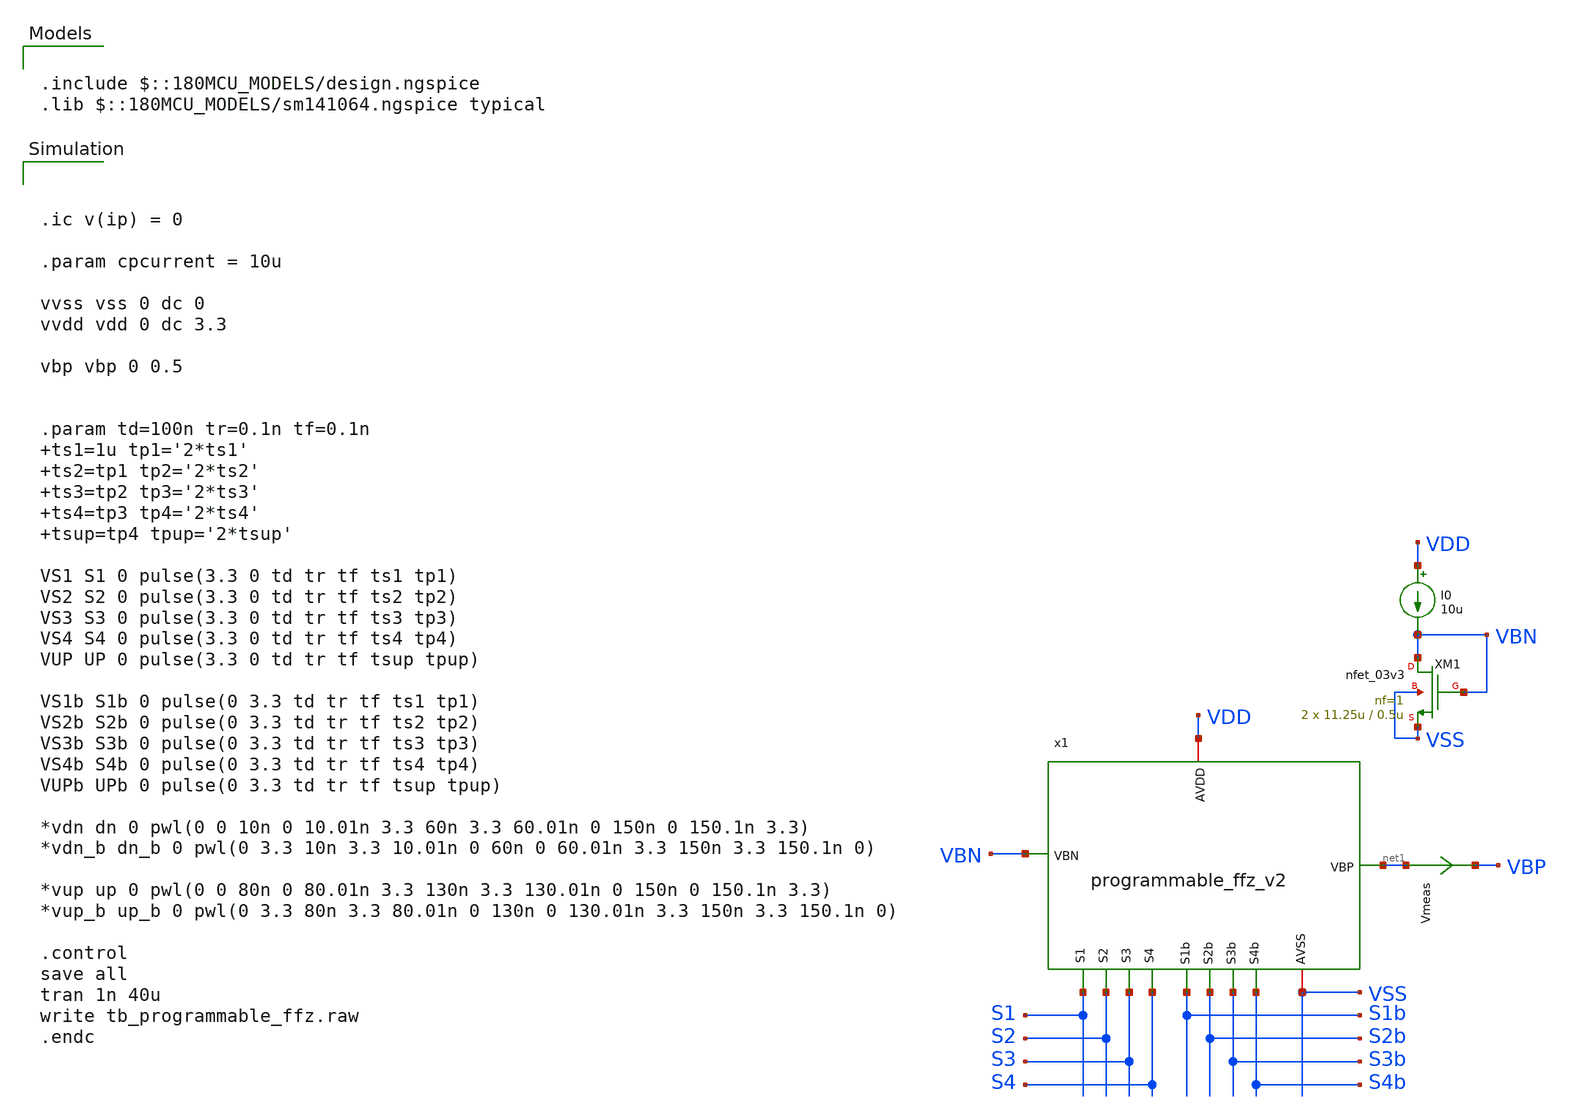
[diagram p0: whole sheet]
** sch_path: designs/libs/tb_analog/tb_programmable_ffz/tb_programmable_ffz_v2.sch
**.subckt tb_programmable_ffz_v2
Vmeas net1 VBP 0
.save i(vmeas)
XM1 VBN VBN VSS VSS nfet_03v3 L=0.5u W=11.25u nf=1 ad='int((nf+1)/2) * W/nf * 0.18u' as='int((nf+2)/2) * W/nf * 0.18u'
+ pd='2*int((nf+1)/2) * (W/nf + 0.18u)' ps='2*int((nf+2)/2) * (W/nf + 0.18u)' nrd='0.18u / W' nrs='0.18u / W'
+ sa=0 sb=0 sd=0 m=2
I0 VDD VBN 10u
x1 VSS VDD net1 VBN S1b S1 S2b S2 S3b S3 S4b S4 programmable_ffz_v2
**** begin user architecture code



.ic v(ip) = 0

.param cpcurrent = 10u

vvss vss 0 dc 0
vvdd vdd 0 dc 3.3

vbp vbp 0 0.5


.param td=100n tr=0.1n tf=0.1n ts1=1u tp1='2*ts1' ts2=tp1 tp2='2*ts2' ts3=tp2 tp3='2*ts3' ts4=tp3 tp4='2*ts4'
+ tsup=tp4 tpup='2*tsup'

VS1 S1 0 pulse(3.3 0 td tr tf ts1 tp1)
VS2 S2 0 pulse(3.3 0 td tr tf ts2 tp2)
VS3 S3 0 pulse(3.3 0 td tr tf ts3 tp3)
VS4 S4 0 pulse(3.3 0 td tr tf ts4 tp4)
VUP UP 0 pulse(3.3 0 td tr tf tsup tpup)

VS1b S1b 0 pulse(0 3.3 td tr tf ts1 tp1)
VS2b S2b 0 pulse(0 3.3 td tr tf ts2 tp2)
VS3b S3b 0 pulse(0 3.3 td tr tf ts3 tp3)
VS4b S4b 0 pulse(0 3.3 td tr tf ts4 tp4)
VUPb UPb 0 pulse(0 3.3 td tr tf tsup tpup)

*vdn dn 0 pwl(0 0 10n 0 10.01n 3.3 60n 3.3 60.01n 0 150n 0 150.1n 3.3)
*vdn_b dn_b 0 pwl(0 3.3 10n 3.3 10.01n 0 60n 0 60.01n 3.3 150n 3.3 150.1n 0)

*vup up 0 pwl(0 0 80n 0 80.01n 3.3 130n 3.3 130.01n 0 150n 0 150.1n 3.3)
*vup_b up_b 0 pwl(0 3.3 80n 3.3 80.01n 0 130n 0 130.01n 3.3 150n 3.3 150.1n 0)

.control
save all
tran 1n 40u
write tb_programmable_ffz.raw
.endc



.include $::180MCU_MODELS/design.ngspice
.lib $::180MCU_MODELS/sm141064.ngspice typical

**** end user architecture code
**.ends

* expanding   symbol:  libs/core_analog/programmable_ffz/programmable_ffz_v2.sym # of pins=12
** sym_path: designs/libs/core_analog/programmable_ffz/programmable_ffz_v2.sym
** sch_path: designs/libs/core_analog/programmable_ffz/programmable_ffz_v2.sch
.subckt programmable_ffz_v2 AVSS AVDD VBP VBN S1b S1 S2b S2 S3b S3 S4b S4
*.ipin VBN
*.ipin S1b
*.ipin S1
*.ipin S2b
*.ipin S2
*.ipin S3b
*.ipin S3
*.ipin S4b
*.ipin S4
*.iopin AVSS
*.iopin AVDD
*.opin VBP
x2 VBN AVSS S1 VBN1 S1b AVDD transmission_gate
x3 VBN AVSS S2 VBN2 S2b AVDD transmission_gate
x4 VBN AVSS S3 VBN3 S3b AVDD transmission_gate
x5 VBN AVSS S4 VBN4 S4b AVDD transmission_gate
x7 VBP_B AVSS S1 VBP S1b AVDD transmission_gate
x81 VBP_C AVSS S2 VBP S2b AVDD transmission_gate
x82 VBP_C AVSS S2 VBP S2b AVDD transmission_gate
x91 VBP_D AVSS S3 VBP S3b AVDD transmission_gate
x92 VBP_D AVSS S3 VBP S3b AVDD transmission_gate
x93 VBP_D AVSS S3 VBP S3b AVDD transmission_gate
x94 VBP_D AVSS S3 VBP S3b AVDD transmission_gate
x101 VBP_E AVSS S4 VBP S4b AVDD transmission_gate
x102 VBP_E AVSS S4 VBP S4b AVDD transmission_gate
x103 VBP_E AVSS S4 VBP S4b AVDD transmission_gate
x104 VBP_E AVSS S4 VBP S4b AVDD transmission_gate
x105 VBP_E AVSS S4 VBP S4b AVDD transmission_gate
x106 VBP_E AVSS S4 VBP S4b AVDD transmission_gate
x107 VBP_E AVSS S4 VBP S4b AVDD transmission_gate
x108 VBP_E AVSS S4 VBP S4b AVDD transmission_gate
x8 VBP_E VBP VBP_C VBN4 VBN VBN2 S4b AVSS S2b AVDD AVSS VBP_B VBP_D VBN1 VBN3 S3b S1b
+ feed_forward_zero_v2_merged
.ends


* expanding   symbol:  libs/core_analog/transmission_gate/transmission_gate.sym # of pins=6
** sym_path: designs/libs/core_analog/transmission_gate/transmission_gate.sym
** sch_path: designs/libs/core_analog/transmission_gate/transmission_gate.sch
.subckt transmission_gate ind vss clkn ins clkp vdd
*.iopin ind
*.iopin ins
*.iopin clkn
*.iopin clkp
*.iopin vdd
*.iopin vss
XM1 ind clkp ins vdd pfet_03v3 L=0.5u W=3.0u nf=1 ad='int((nf+1)/2) * W/nf * 0.18u' as='int((nf+2)/2) * W/nf * 0.18u'
+ pd='2*int((nf+1)/2) * (W/nf + 0.18u)' ps='2*int((nf+2)/2) * (W/nf + 0.18u)' nrd='0.18u / W' nrs='0.18u / W'
+ sa=0 sb=0 sd=0 m=1
XM2 ind clkn ins vss nfet_03v3 L=0.5u W=1.0u nf=1 ad='int((nf+1)/2) * W/nf * 0.18u' as='int((nf+2)/2) * W/nf * 0.18u'
+ pd='2*int((nf+1)/2) * (W/nf + 0.18u)' ps='2*int((nf+2)/2) * (W/nf + 0.18u)' nrd='0.18u / W' nrs='0.18u / W'
+ sa=0 sb=0 sd=0 m=1
.ends


* expanding   symbol:  libs/core_analog/feed_forward_zero/feed_forward_zero_v2_merged.sym # of
*+ pins=17
** sym_path: designs/libs/core_analog/feed_forward_zero/feed_forward_zero_v2_merged.sym
** sch_path: designs/libs/core_analog/feed_forward_zero/feed_forward_zero_v2_merged.sch
.subckt feed_forward_zero_v2_merged VBP_E VBP_A VBP_C VBN_E VBN_A VBN_C S_E S_A S_C AVDD AVSS VBP_B
+ VBP_D VBN_B VBN_D S_D S_B
*.opin VBP_E
*.iopin AVDD
*.ipin VBN_A
*.opin VBP_A
*.ipin VBN_B
*.ipin S_B
*.opin VBP_B
*.ipin VBN_C
*.ipin S_C
*.opin VBP_C
*.ipin VBN_D
*.ipin S_D
*.opin VBP_D
*.ipin VBN_E
*.ipin S_E
*.ipin S_A
*.iopin AVSS
XM1 VBP_A VBP_A AVDD AVDD pfet_03v3 L=1.5u W=1.1u nf=1 ad='int((nf+1)/2) * W/nf * 0.18u' as='int((nf+2)/2) * W/nf * 0.18u'
+ pd='2*int((nf+1)/2) * (W/nf + 0.18u)' ps='2*int((nf+2)/2) * (W/nf + 0.18u)' nrd='0.18u / W' nrs='0.18u / W'
+ sa=0 sb=0 sd=0 m=1
XM3 VBP_A AVDD net1 AVSS nfet_03v3 L=0.5u W=2.08u nf=1 ad='int((nf+1)/2) * W/nf * 0.18u' as='int((nf+2)/2) * W/nf * 0.18u'
+ pd='2*int((nf+1)/2) * (W/nf + 0.18u)' ps='2*int((nf+2)/2) * (W/nf + 0.18u)' nrd='0.18u / W' nrs='0.18u / W'
+ sa=0 sb=0 sd=0 m=1
XM4 net1 VBN_A AVSS AVSS nfet_03v3 L=0.5u W=2.82u nf=1 ad='int((nf+1)/2) * W/nf * 0.18u' as='int((nf+2)/2) * W/nf * 0.18u'
+ pd='2*int((nf+1)/2) * (W/nf + 0.18u)' ps='2*int((nf+2)/2) * (W/nf + 0.18u)' nrd='0.18u / W' nrs='0.18u / W'
+ sa=0 sb=0 sd=0 m=4
XM7 VBN_A S_A AVSS AVSS nfet_03v3 L=0.5u W=1u nf=1 ad='int((nf+1)/2) * W/nf * 0.18u' as='int((nf+2)/2) * W/nf * 0.18u'
+ pd='2*int((nf+1)/2) * (W/nf + 0.18u)' ps='2*int((nf+2)/2) * (W/nf + 0.18u)' nrd='0.18u / W' nrs='0.18u / W'
+ sa=0 sb=0 sd=0 m=1
XM2 VBP_A VBP_A AVDD AVDD pfet_03v3 L=1.5u W=1.1u nf=1 ad='int((nf+1)/2) * W/nf * 0.18u' as='int((nf+2)/2) * W/nf * 0.18u'
+ pd='2*int((nf+1)/2) * (W/nf + 0.18u)' ps='2*int((nf+2)/2) * (W/nf + 0.18u)' nrd='0.18u / W' nrs='0.18u / W'
+ sa=0 sb=0 sd=0 m=1
XM5 VBP_B VBP_B AVDD AVDD pfet_03v3 L=1.5u W=1.1u nf=1 ad='int((nf+1)/2) * W/nf * 0.18u' as='int((nf+2)/2) * W/nf * 0.18u'
+ pd='2*int((nf+1)/2) * (W/nf + 0.18u)' ps='2*int((nf+2)/2) * (W/nf + 0.18u)' nrd='0.18u / W' nrs='0.18u / W'
+ sa=0 sb=0 sd=0 m=1
XM6 VBP_B AVDD net2 AVSS nfet_03v3 L=0.5u W=2.08u nf=1 ad='int((nf+1)/2) * W/nf * 0.18u' as='int((nf+2)/2) * W/nf * 0.18u'
+ pd='2*int((nf+1)/2) * (W/nf + 0.18u)' ps='2*int((nf+2)/2) * (W/nf + 0.18u)' nrd='0.18u / W' nrs='0.18u / W'
+ sa=0 sb=0 sd=0 m=1
XM8 net2 VBN_B AVSS AVSS nfet_03v3 L=0.5u W=2.82u nf=1 ad='int((nf+1)/2) * W/nf * 0.18u' as='int((nf+2)/2) * W/nf * 0.18u'
+ pd='2*int((nf+1)/2) * (W/nf + 0.18u)' ps='2*int((nf+2)/2) * (W/nf + 0.18u)' nrd='0.18u / W' nrs='0.18u / W'
+ sa=0 sb=0 sd=0 m=4
XM9 VBN_B S_B AVSS AVSS nfet_03v3 L=0.5u W=1u nf=1 ad='int((nf+1)/2) * W/nf * 0.18u' as='int((nf+2)/2) * W/nf * 0.18u'
+ pd='2*int((nf+1)/2) * (W/nf + 0.18u)' ps='2*int((nf+2)/2) * (W/nf + 0.18u)' nrd='0.18u / W' nrs='0.18u / W'
+ sa=0 sb=0 sd=0 m=1
XM10 VBP_B VBP_B AVDD AVDD pfet_03v3 L=1.5u W=1.1u nf=1 ad='int((nf+1)/2) * W/nf * 0.18u' as='int((nf+2)/2) * W/nf * 0.18u'
+ pd='2*int((nf+1)/2) * (W/nf + 0.18u)' ps='2*int((nf+2)/2) * (W/nf + 0.18u)' nrd='0.18u / W' nrs='0.18u / W'
+ sa=0 sb=0 sd=0 m=1
XM11 VBP_C VBP_C AVDD AVDD pfet_03v3 L=1.5u W=1.1u nf=1 ad='int((nf+1)/2) * W/nf * 0.18u' as='int((nf+2)/2) * W/nf * 0.18u'
+ pd='2*int((nf+1)/2) * (W/nf + 0.18u)' ps='2*int((nf+2)/2) * (W/nf + 0.18u)' nrd='0.18u / W' nrs='0.18u / W'
+ sa=0 sb=0 sd=0 m=2
XM12 VBP_C AVDD net3 AVSS nfet_03v3 L=0.5u W=2.08u nf=1 ad='int((nf+1)/2) * W/nf * 0.18u' as='int((nf+2)/2) * W/nf * 0.18u'
+ pd='2*int((nf+1)/2) * (W/nf + 0.18u)' ps='2*int((nf+2)/2) * (W/nf + 0.18u)' nrd='0.18u / W' nrs='0.18u / W'
+ sa=0 sb=0 sd=0 m=2
XM13 net3 VBN_C AVSS AVSS nfet_03v3 L=0.5u W=2.82u nf=1 ad='int((nf+1)/2) * W/nf * 0.18u' as='int((nf+2)/2) * W/nf * 0.18u'
+ pd='2*int((nf+1)/2) * (W/nf + 0.18u)' ps='2*int((nf+2)/2) * (W/nf + 0.18u)' nrd='0.18u / W' nrs='0.18u / W'
+ sa=0 sb=0 sd=0 m=8
XM14 VBN_C S_C AVSS AVSS nfet_03v3 L=0.5u W=1u nf=1 ad='int((nf+1)/2) * W/nf * 0.18u' as='int((nf+2)/2) * W/nf * 0.18u'
+ pd='2*int((nf+1)/2) * (W/nf + 0.18u)' ps='2*int((nf+2)/2) * (W/nf + 0.18u)' nrd='0.18u / W' nrs='0.18u / W'
+ sa=0 sb=0 sd=0 m=2
XM15 VBP_C VBP_C AVDD AVDD pfet_03v3 L=1.5u W=1.1u nf=1 ad='int((nf+1)/2) * W/nf * 0.18u' as='int((nf+2)/2) * W/nf * 0.18u'
+ pd='2*int((nf+1)/2) * (W/nf + 0.18u)' ps='2*int((nf+2)/2) * (W/nf + 0.18u)' nrd='0.18u / W' nrs='0.18u / W'
+ sa=0 sb=0 sd=0 m=2
XM16 VBP_D VBP_D AVDD AVDD pfet_03v3 L=1.5u W=1.1u nf=1 ad='int((nf+1)/2) * W/nf * 0.18u' as='int((nf+2)/2) * W/nf * 0.18u'
+ pd='2*int((nf+1)/2) * (W/nf + 0.18u)' ps='2*int((nf+2)/2) * (W/nf + 0.18u)' nrd='0.18u / W' nrs='0.18u / W'
+ sa=0 sb=0 sd=0 m=4
XM17 VBP_D AVDD net4 AVSS nfet_03v3 L=0.5u W=2.08u nf=1 ad='int((nf+1)/2) * W/nf * 0.18u' as='int((nf+2)/2) * W/nf * 0.18u'
+ pd='2*int((nf+1)/2) * (W/nf + 0.18u)' ps='2*int((nf+2)/2) * (W/nf + 0.18u)' nrd='0.18u / W' nrs='0.18u / W'
+ sa=0 sb=0 sd=0 m=4
XM18 net4 VBN_D AVSS AVSS nfet_03v3 L=0.5u W=2.82u nf=1 ad='int((nf+1)/2) * W/nf * 0.18u' as='int((nf+2)/2) * W/nf * 0.18u'
+ pd='2*int((nf+1)/2) * (W/nf + 0.18u)' ps='2*int((nf+2)/2) * (W/nf + 0.18u)' nrd='0.18u / W' nrs='0.18u / W'
+ sa=0 sb=0 sd=0 m=16
XM19 VBN_D S_D AVSS AVSS nfet_03v3 L=0.5u W=1u nf=1 ad='int((nf+1)/2) * W/nf * 0.18u' as='int((nf+2)/2) * W/nf * 0.18u'
+ pd='2*int((nf+1)/2) * (W/nf + 0.18u)' ps='2*int((nf+2)/2) * (W/nf + 0.18u)' nrd='0.18u / W' nrs='0.18u / W'
+ sa=0 sb=0 sd=0 m=4
XM20 VBP_D VBP_D AVDD AVDD pfet_03v3 L=1.5u W=1.1u nf=1 ad='int((nf+1)/2) * W/nf * 0.18u' as='int((nf+2)/2) * W/nf * 0.18u'
+ pd='2*int((nf+1)/2) * (W/nf + 0.18u)' ps='2*int((nf+2)/2) * (W/nf + 0.18u)' nrd='0.18u / W' nrs='0.18u / W'
+ sa=0 sb=0 sd=0 m=4
XM21 VBP_E VBP_E AVDD AVDD pfet_03v3 L=1.5u W=1.1u nf=1 ad='int((nf+1)/2) * W/nf * 0.18u' as='int((nf+2)/2) * W/nf * 0.18u'
+ pd='2*int((nf+1)/2) * (W/nf + 0.18u)' ps='2*int((nf+2)/2) * (W/nf + 0.18u)' nrd='0.18u / W' nrs='0.18u / W'
+ sa=0 sb=0 sd=0 m=8
XM22 VBP_E AVDD net5 AVSS nfet_03v3 L=0.5u W=2.08u nf=1 ad='int((nf+1)/2) * W/nf * 0.18u' as='int((nf+2)/2) * W/nf * 0.18u'
+ pd='2*int((nf+1)/2) * (W/nf + 0.18u)' ps='2*int((nf+2)/2) * (W/nf + 0.18u)' nrd='0.18u / W' nrs='0.18u / W'
+ sa=0 sb=0 sd=0 m=8
XM23 net5 VBN_E AVSS AVSS nfet_03v3 L=0.5u W=2.82u nf=1 ad='int((nf+1)/2) * W/nf * 0.18u' as='int((nf+2)/2) * W/nf * 0.18u'
+ pd='2*int((nf+1)/2) * (W/nf + 0.18u)' ps='2*int((nf+2)/2) * (W/nf + 0.18u)' nrd='0.18u / W' nrs='0.18u / W'
+ sa=0 sb=0 sd=0 m=32
XM24 VBN_E S_E AVSS AVSS nfet_03v3 L=0.5u W=1u nf=1 ad='int((nf+1)/2) * W/nf * 0.18u' as='int((nf+2)/2) * W/nf * 0.18u'
+ pd='2*int((nf+1)/2) * (W/nf + 0.18u)' ps='2*int((nf+2)/2) * (W/nf + 0.18u)' nrd='0.18u / W' nrs='0.18u / W'
+ sa=0 sb=0 sd=0 m=8
XM25 VBP_E VBP_E AVDD AVDD pfet_03v3 L=1.5u W=1.1u nf=1 ad='int((nf+1)/2) * W/nf * 0.18u' as='int((nf+2)/2) * W/nf * 0.18u'
+ pd='2*int((nf+1)/2) * (W/nf + 0.18u)' ps='2*int((nf+2)/2) * (W/nf + 0.18u)' nrd='0.18u / W' nrs='0.18u / W'
+ sa=0 sb=0 sd=0 m=8
.ends

.end
